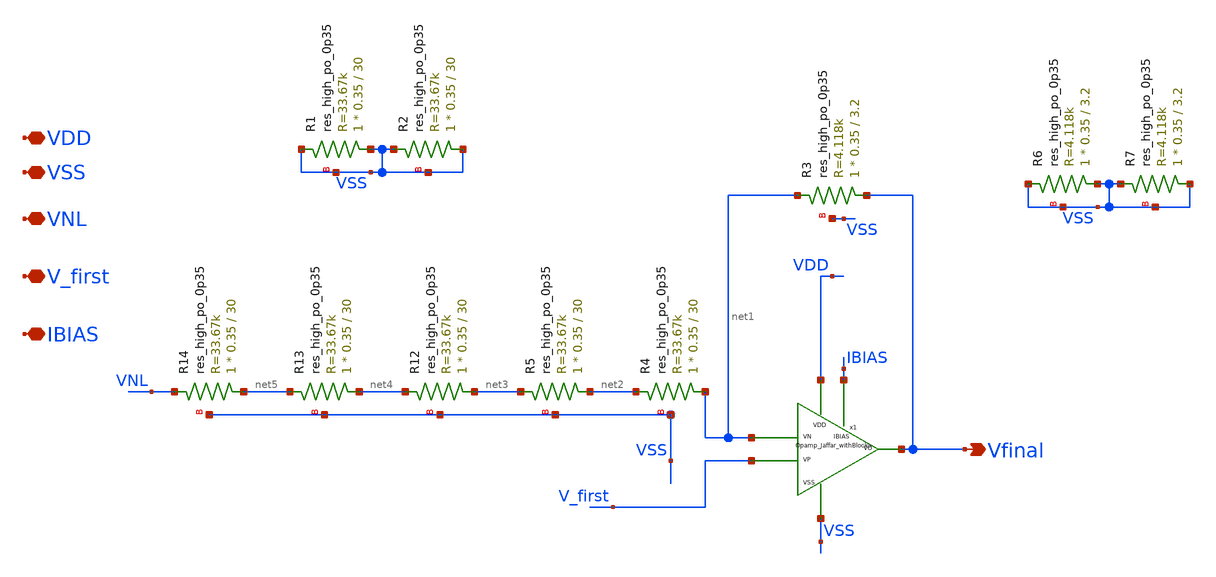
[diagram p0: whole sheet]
** sch_path: xschem/xschem_BGR_Top/BGR_2ndc.sch
**.subckt BGR_2ndc Vfinal VNL V_first IBIAS VSS VDD
*.opin Vfinal
*.iopin VNL
*.iopin V_first
*.iopin IBIAS
*.iopin VSS
*.iopin VDD
XR3 Vfinal net1 VSS sky130_fd_pr__res_high_po_0p35 L=3.2 mult=1 m=1
XR4 net1 net2 VSS sky130_fd_pr__res_high_po_0p35 L=30 mult=1 m=1
XR5 net2 net3 VSS sky130_fd_pr__res_high_po_0p35 L=30 mult=1 m=1
XR12 net3 net4 VSS sky130_fd_pr__res_high_po_0p35 L=30 mult=1 m=1
XR13 net4 net5 VSS sky130_fd_pr__res_high_po_0p35 L=30 mult=1 m=1
XR14 net5 VNL VSS sky130_fd_pr__res_high_po_0p35 L=30 mult=1 m=1
XR1 VSS VSS VSS sky130_fd_pr__res_high_po_0p35 L=30 mult=1 m=1
XR2 VSS VSS VSS sky130_fd_pr__res_high_po_0p35 L=30 mult=1 m=1
XR6 VSS VSS VSS sky130_fd_pr__res_high_po_0p35 L=3.2 mult=1 m=1
XR7 VSS VSS VSS sky130_fd_pr__res_high_po_0p35 L=3.2 mult=1 m=1
x1 VDD VSS V_first net1 Vfinal IBIAS Opamp_Jaffar_withBlocks
**.ends
.end
